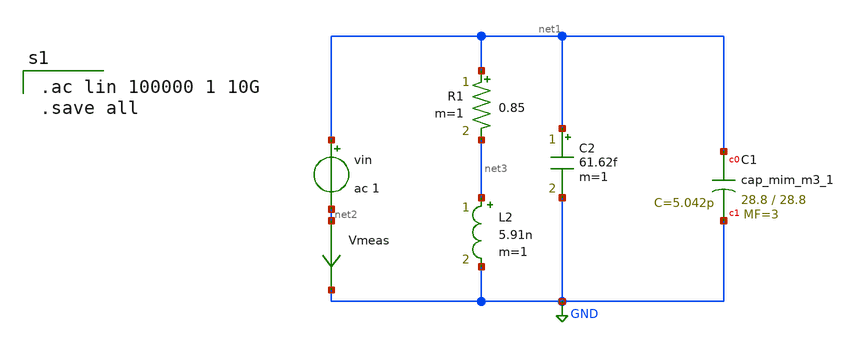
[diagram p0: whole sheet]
** sch_path: XSCHEM/ANTENNA/RLC_CSTXschem400.sch
**.subckt RLC_CSTXschem400
vin net1 net2 ac 1
XC1 net1 GND sky130_fd_pr__cap_mim_m3_1 W=28.8 L=28.8 MF=3 m=3
Vmeas net2 GND 0
.save i(vmeas)
R1 net1 net3 0.85 m=1
L2 net3 GND 5.91n m=1
C2 net1 GND 61.62f m=1
**** begin user architecture code

.ac lin 100000 1 10G
.save all


** opencircuitdesign pdks install
.lib $::SKYWATER_MODELS/sky130.lib.spice ff
.include /usr/local/share/pdk/sky130A/libs.ref/sky130_fd_sc_hd/spice/sky130_fd_sc_hd.spice

**** end user architecture code
**.ends
.GLOBAL GND
.end
